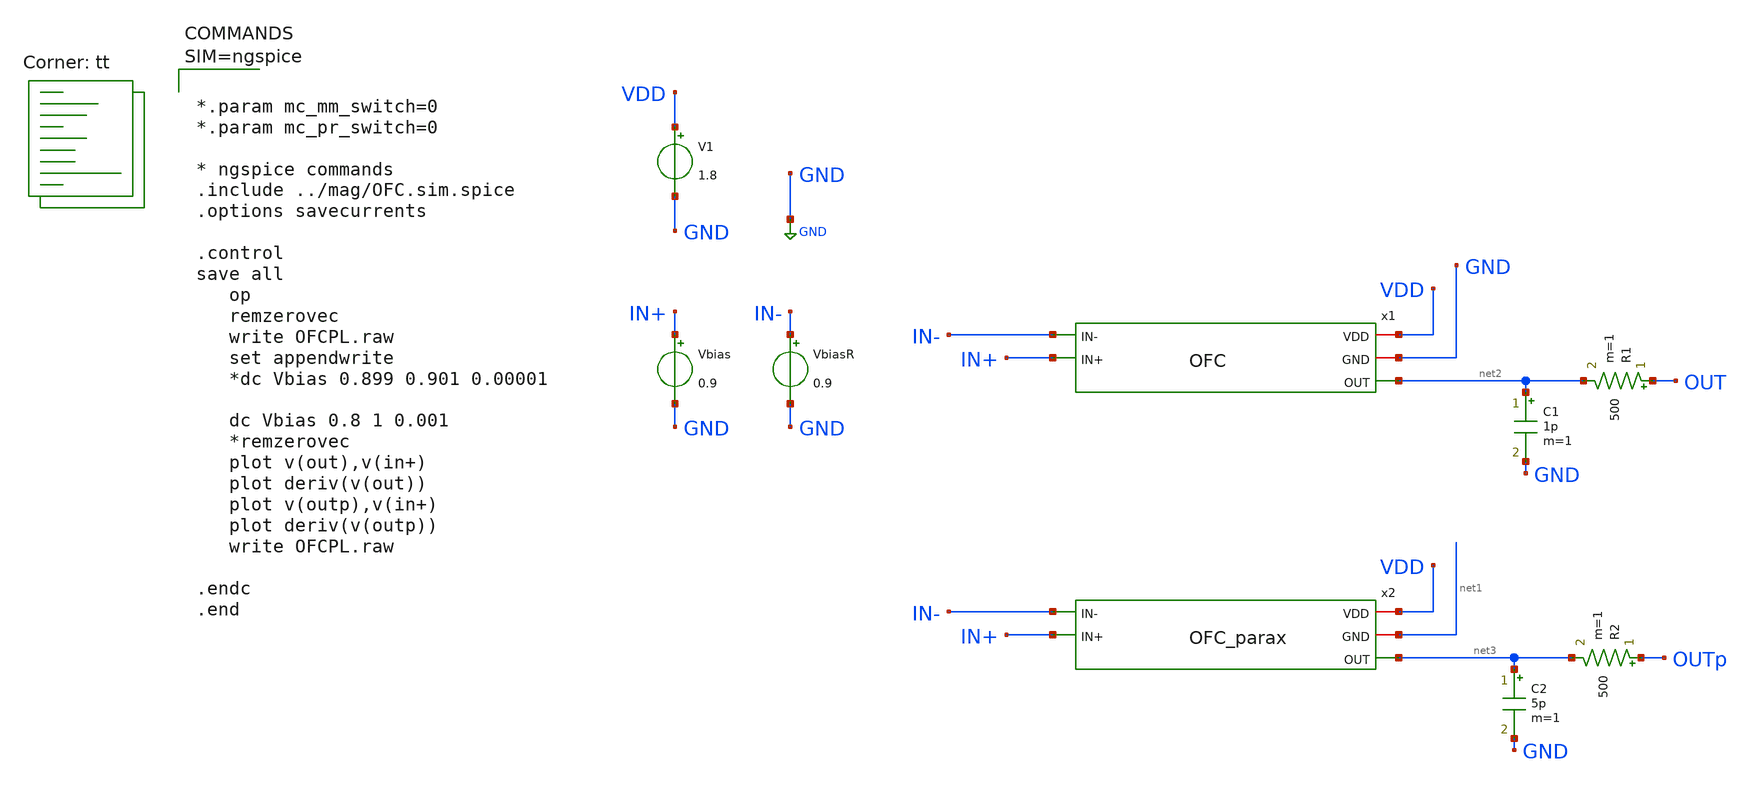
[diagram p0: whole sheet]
** sch_path: xschem/OFCPL.sch
**.subckt OFCPL
x1 VDD GND net2 IN- IN+ OFC
x2 VDD net1 net3 IN- IN+ OFC_parax
V1 VDD GND 1.8
Vbias IN+ GND 0.9
VbiasR IN- GND 0.9
R1 OUT net2 500 m=1
C1 net2 GND 1p m=1
R2 OUTp net3 500 m=1
C2 net3 GND 5p m=1
**** begin user architecture code



*.param mc_mm_switch=0
*.param mc_pr_switch=0

* ngspice commands
.include ../mag/OFC.sim.spice
.options savecurrents

.control
save all
   op
   remzerovec
   write OFCPL.raw
   set appendwrite
   *dc Vbias 0.899 0.901 0.00001

   dc Vbias 0.8 1 0.001
   *remzerovec
   plot v(out),v(in+)
   plot deriv(v(out))
   plot v(outp),v(in+)
   plot deriv(v(outp))
   write OFCPL.raw

.endc
.end



.lib $::SKYWATER_MODELS/sky130.lib.spice tt
**** end user architecture code
**.ends

* expanding   symbol:  OFC.sym # of pins=5
** sym_path: xschem/OFC.sym
** sch_path: xschem/OFC.sch
.subckt OFC VDD GND OUT IN- IN+
*.iopin VDD
*.iopin GND
*.ipin IN+
*.ipin IN-
*.opin OUT
XM1 D1 IN+ S S sky130_fd_pr__pfet_01v8 L=1 W=10 nf=1 ad='int((nf+1)/2) * W/nf * 0.29' as='int((nf+2)/2) * W/nf * 0.29'
+ pd='2*int((nf+1)/2) * (W/nf + 0.29)' ps='2*int((nf+2)/2) * (W/nf + 0.29)' nrd='0.29 / W' nrs='0.29 / W'
+ sa=0 sb=0 sd=0 mult=5 m=5
XM2 D2 IN- S S sky130_fd_pr__pfet_01v8 L=1 W=10 nf=1 ad='int((nf+1)/2) * W/nf * 0.29' as='int((nf+2)/2) * W/nf * 0.29'
+ pd='2*int((nf+1)/2) * (W/nf + 0.29)' ps='2*int((nf+2)/2) * (W/nf + 0.29)' nrd='0.29 / W' nrs='0.29 / W'
+ sa=0 sb=0 sd=0 mult=5 m=5
XM3 D1 Vc GND GND sky130_fd_pr__nfet_01v8 L=10 W=2 nf=1 ad='int((nf+1)/2) * W/nf * 0.29' as='int((nf+2)/2) * W/nf * 0.29'
+ pd='2*int((nf+1)/2) * (W/nf + 0.29)' ps='2*int((nf+2)/2) * (W/nf + 0.29)' nrd='0.29 / W' nrs='0.29 / W'
+ sa=0 sb=0 sd=0 mult=1 m=1
XM4 D2 Vc GND GND sky130_fd_pr__nfet_01v8 L=10 W=2 nf=1 ad='int((nf+1)/2) * W/nf * 0.29' as='int((nf+2)/2) * W/nf * 0.29'
+ pd='2*int((nf+1)/2) * (W/nf + 0.29)' ps='2*int((nf+2)/2) * (W/nf + 0.29)' nrd='0.29 / W' nrs='0.29 / W'
+ sa=0 sb=0 sd=0 mult=1 m=1
XM5 G Vc D1 GND sky130_fd_pr__nfet_01v8 L=2 W=3 nf=1 ad='int((nf+1)/2) * W/nf * 0.29' as='int((nf+2)/2) * W/nf * 0.29'
+ pd='2*int((nf+1)/2) * (W/nf + 0.29)' ps='2*int((nf+2)/2) * (W/nf + 0.29)' nrd='0.29 / W' nrs='0.29 / W'
+ sa=0 sb=0 sd=0 mult=1 m=1
XM6 OUT Vc D2 GND sky130_fd_pr__nfet_01v8 L=2 W=3 nf=1 ad='int((nf+1)/2) * W/nf * 0.29' as='int((nf+2)/2) * W/nf * 0.29'
+ pd='2*int((nf+1)/2) * (W/nf + 0.29)' ps='2*int((nf+2)/2) * (W/nf + 0.29)' nrd='0.29 / W' nrs='0.29 / W'
+ sa=0 sb=0 sd=0 mult=1 m=1
XM7 G Vc D9 D9 sky130_fd_pr__pfet_01v8 L=5 W=10 nf=1 ad='int((nf+1)/2) * W/nf * 0.29' as='int((nf+2)/2) * W/nf * 0.29'
+ pd='2*int((nf+1)/2) * (W/nf + 0.29)' ps='2*int((nf+2)/2) * (W/nf + 0.29)' nrd='0.29 / W' nrs='0.29 / W'
+ sa=0 sb=0 sd=0 mult=1 m=1
XM8 OUT Vc D10 D10 sky130_fd_pr__pfet_01v8 L=5 W=10 nf=1 ad='int((nf+1)/2) * W/nf * 0.29' as='int((nf+2)/2) * W/nf * 0.29'
+ pd='2*int((nf+1)/2) * (W/nf + 0.29)' ps='2*int((nf+2)/2) * (W/nf + 0.29)' nrd='0.29 / W' nrs='0.29 / W'
+ sa=0 sb=0 sd=0 mult=1 m=1
XM9 D9 G VDD VDD sky130_fd_pr__pfet_01v8 L=1 W=25.5 nf=1 ad='int((nf+1)/2) * W/nf * 0.29' as='int((nf+2)/2) * W/nf * 0.29'
+ pd='2*int((nf+1)/2) * (W/nf + 0.29)' ps='2*int((nf+2)/2) * (W/nf + 0.29)' nrd='0.29 / W' nrs='0.29 / W'
+ sa=0 sb=0 sd=0 mult=1 m=1
XM10 D10 G VDD VDD sky130_fd_pr__pfet_01v8 L=1 W=25.5 nf=1 ad='int((nf+1)/2) * W/nf * 0.29' as='int((nf+2)/2) * W/nf * 0.29'
+ pd='2*int((nf+1)/2) * (W/nf + 0.29)' ps='2*int((nf+2)/2) * (W/nf + 0.29)' nrd='0.29 / W' nrs='0.29 / W'
+ sa=0 sb=0 sd=0 mult=1 m=1
XM11 S Vp net1 VDD sky130_fd_pr__pfet_01v8 L=5 W=5 nf=1 ad='int((nf+1)/2) * W/nf * 0.29' as='int((nf+2)/2) * W/nf * 0.29'
+ pd='2*int((nf+1)/2) * (W/nf + 0.29)' ps='2*int((nf+2)/2) * (W/nf + 0.29)' nrd='0.29 / W' nrs='0.29 / W'
+ sa=0 sb=0 sd=0 mult=1 m=1
XM12 net1 Vp VDD VDD sky130_fd_pr__pfet_01v8 L=5 W=5 nf=1 ad='int((nf+1)/2) * W/nf * 0.29' as='int((nf+2)/2) * W/nf * 0.29'
+ pd='2*int((nf+1)/2) * (W/nf + 0.29)' ps='2*int((nf+2)/2) * (W/nf + 0.29)' nrd='0.29 / W' nrs='0.29 / W'
+ sa=0 sb=0 sd=0 mult=1 m=1
XR5 Vc VDD GND sky130_fd_pr__res_xhigh_po_0p35 L=5 mult=1 m=1
XR1 GND Vc GND sky130_fd_pr__res_xhigh_po_0p35 L=3.15 mult=1 m=1
XR2 Vp VDD GND sky130_fd_pr__res_xhigh_po_0p35 L=5 mult=1 m=1
XR3 GND Vp GND sky130_fd_pr__res_xhigh_po_0p35 L=1.86 mult=1 m=1
.ends


* expanding   symbol:  OFC_parax.sym # of pins=5
** sym_path: xschem/OFC.sym
.include [file normalize ../mag/OFC.sim.spice]
.GLOBAL GND
.end
